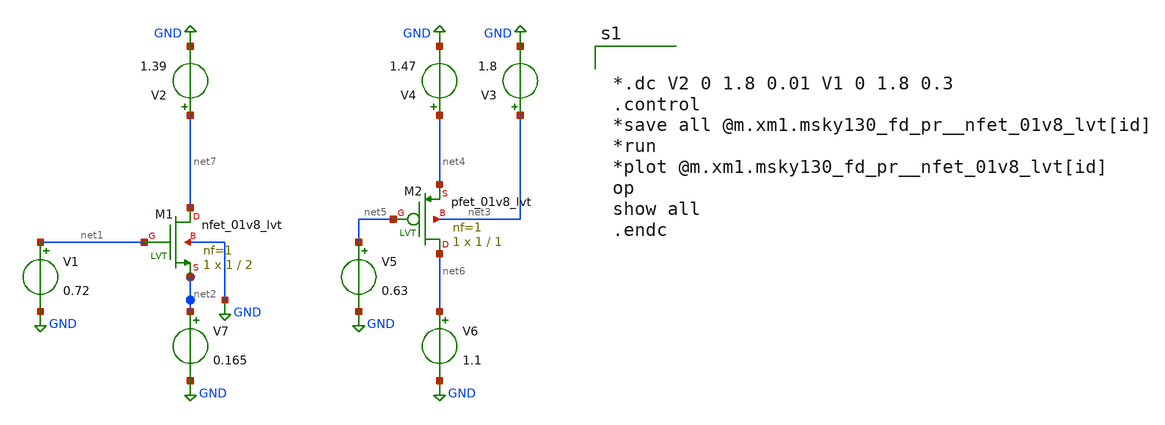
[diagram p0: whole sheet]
** sch_path: untitled.sch
**.subckt untitled
XM1 net7 net1 net2 GND sky130_fd_pr__nfet_01v8_lvt L=2 W=1 nf=1 ad='int((nf+1)/2) * W/nf * 0.29' as='int((nf+2)/2) * W/nf * 0.29'
+ pd='2*int((nf+1)/2) * (W/nf + 0.29)' ps='2*int((nf+2)/2) * (W/nf + 0.29)' nrd='0.29 / W' nrs='0.29 / W'
+ sa=0 sb=0 sd=0 mult=1 m=1
XM2 net6 net5 net4 net3 sky130_fd_pr__pfet_01v8_lvt L=1 W=1 nf=1 ad='int((nf+1)/2) * W/nf * 0.29' as='int((nf+2)/2) * W/nf * 0.29'
+ pd='2*int((nf+1)/2) * (W/nf + 0.29)' ps='2*int((nf+2)/2) * (W/nf + 0.29)' nrd='0.29 / W' nrs='0.29 / W'
+ sa=0 sb=0 sd=0 mult=1 m=1
V3 net3 GND 1.8
V4 net4 GND 1.47
V5 net5 GND 0.63
V6 net6 GND 1.1
V7 net2 GND 0.165
V1 net1 GND 0.72
V2 net7 GND 1.39
**** begin user architecture code

.lib ~/open_pdks/sky130/sky130A/libs.tech/ngspice/sky130.lib.spice fs


*.dc V2 0 1.8 0.01 V1 0 1.8 0.3
.control
*save all @m.xm1.msky130_fd_pr__nfet_01v8_lvt[id]
*run
*plot @m.xm1.msky130_fd_pr__nfet_01v8_lvt[id]
op
show all
.endc

**** end user architecture code
**.ends
.GLOBAL GND
.end
